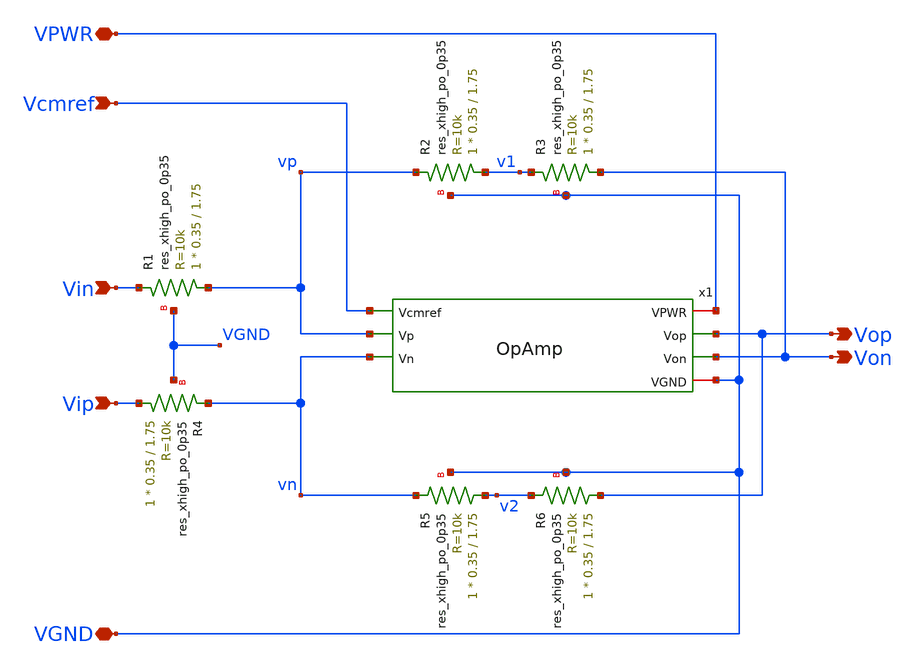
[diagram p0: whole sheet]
** sch_path: Circuits/Examples/InvAmp/InvAmp.sch
**.subckt InvAmp VPWR VGND Vcmref Vin Vip Vop Von
*.iopin VPWR
*.iopin VGND
*.ipin Vcmref
*.ipin Vin
*.ipin Vip
*.opin Vop
*.opin Von
x1 VPWR Vcmref Vop Von vp vn VGND OpAmp
XR1 vp Vin VGND sky130_fd_pr__res_xhigh_po_0p35 L=1.75 mult=1 m=1
XR2 v1 vp VGND sky130_fd_pr__res_xhigh_po_0p35 L=1.75 mult=1 m=1
XR3 Von v1 VGND sky130_fd_pr__res_xhigh_po_0p35 L=1.75 mult=1 m=1
XR4 Vip vn VGND sky130_fd_pr__res_xhigh_po_0p35 L=1.75 mult=1 m=1
XR6 Vop v2 VGND sky130_fd_pr__res_xhigh_po_0p35 L=1.75 mult=1 m=1
XR5 v2 vn VGND sky130_fd_pr__res_xhigh_po_0p35 L=1.75 mult=1 m=1
**.ends

* expanding   symbol:  /home/jakob/Documents/RALF/Circuits/Examples/OpAmp/OpAmp.sym # of pins=7
** sym_path: Circuits/Examples/OpAmp/OpAmp.sym
** sch_path: Circuits/Examples/OpAmp/OpAmp.sch
.subckt OpAmp VPWR Vcmref Vop Von Vp Vn VGND
*.opin Von
*.opin Vop
*.ipin Vcmref
*.ipin Vp
*.ipin Vn
*.iopin VPWR
*.iopin VGND
x2 VPWR Vcmref Von vcmfb Vop vbias VGND CMMFeedback
x3 VPWR vbias VGND GmBias
x1 VPWR Von vcmfb Vp Vn vbias vbias Vop VGND MillerOpAmp
.ends


* expanding   symbol:  /home/jakob/Documents/RALF/Circuits/Examples/OpAmp/CMMFeedback.sym # of
*+ pins=7
** sym_path: Circuits/Examples/OpAmp/CMMFeedback.sym
** sch_path: Circuits/Examples/OpAmp/CMMFeedback.sch
.subckt CMMFeedback Vdd Vcmref Vp Vout Vn Vbdan Vss
*.ipin Vbdan
*.opin Vout
*.ipin Vp
*.ipin Vcmref
*.ipin Vn
*.iopin Vss
*.iopin Vdd
XR1 Vp net1 Vss sky130_fd_pr__res_xhigh_po_0p35 L=3.5 mult=1 m=1
XR2 net1 net2 Vss sky130_fd_pr__res_xhigh_po_0p35 L=3.5 mult=1 m=1
XR3 net2 net3 Vss sky130_fd_pr__res_xhigh_po_0p35 L=3.5 mult=1 m=1
XR4 net3 net4 Vss sky130_fd_pr__res_xhigh_po_0p35 L=3.5 mult=1 m=1
XR5 net4 vcmi Vss sky130_fd_pr__res_xhigh_po_0p35 L=3.5 mult=1 m=1
XR6 Vn net5 Vss sky130_fd_pr__res_xhigh_po_0p35 L=3.5 mult=1 m=1
XR10 net5 net6 Vss sky130_fd_pr__res_xhigh_po_0p35 L=3.5 mult=1 m=1
XR9 net6 net7 Vss sky130_fd_pr__res_xhigh_po_0p35 L=3.5 mult=1 m=1
XR8 net7 net8 Vss sky130_fd_pr__res_xhigh_po_0p35 L=3.5 mult=1 m=1
XR7 net8 vcmi Vss sky130_fd_pr__res_xhigh_po_0p35 L=3.5 mult=1 m=1
x1 Vdd vdts Vout vdts Vcmref vcmi Vbdan Vss DiffAmp
.ends


* expanding   symbol:  /home/jakob/Documents/RALF/Circuits/Examples/OpAmp/GmBias.sym # of pins=3
** sym_path: Circuits/Examples/OpAmp/GmBias.sym
** sch_path: Circuits/Examples/OpAmp/GmBias.sch
.subckt GmBias Vdd Vbias Vss
*.opin Vbias
*.iopin Vss
*.iopin Vdd
XM6 Vbias Vbias Vss Vss sky130_fd_pr__nfet_01v8 L=2 W=1 nf=1 ad='int((nf+1)/2) * W/nf * 0.29' as='int((nf+2)/2) * W/nf * 0.29'
+ pd='2*int((nf+1)/2) * (W/nf + 0.29)' ps='2*int((nf+2)/2) * (W/nf + 0.29)' nrd='0.29 / W' nrs='0.29 / W'
+ sa=0 sb=0 sd=0 mult=1 m=1
XM2 v1 v1 Vdd Vdd sky130_fd_pr__pfet_01v8 L=1 W=4 nf=2 ad='int((nf+1)/2) * W/nf * 0.29' as='int((nf+2)/2) * W/nf * 0.29'
+ pd='2*int((nf+1)/2) * (W/nf + 0.29)' ps='2*int((nf+2)/2) * (W/nf + 0.29)' nrd='0.29 / W' nrs='0.29 / W'
+ sa=0 sb=0 sd=0 mult=1 m=1
XM1 Vbias v1 Vdd Vdd sky130_fd_pr__pfet_01v8 L=1 W=4 nf=2 ad='int((nf+1)/2) * W/nf * 0.29' as='int((nf+2)/2) * W/nf * 0.29'
+ pd='2*int((nf+1)/2) * (W/nf + 0.29)' ps='2*int((nf+2)/2) * (W/nf + 0.29)' nrd='0.29 / W' nrs='0.29 / W'
+ sa=0 sb=0 sd=0 mult=1 m=1
XM3 v1 Vbias net1 Vss sky130_fd_pr__nfet_01v8 L=2 W=1 nf=1 ad='int((nf+1)/2) * W/nf * 0.29' as='int((nf+2)/2) * W/nf * 0.29'
+ pd='2*int((nf+1)/2) * (W/nf + 0.29)' ps='2*int((nf+2)/2) * (W/nf + 0.29)' nrd='0.29 / W' nrs='0.29 / W'
+ sa=0 sb=0 sd=0 mult=1 m=1
XR6 Vss net1 Vss sky130_fd_pr__res_xhigh_po_0p35 L=1 mult=1 m=1
XM4 v1 v1 Vbias Vss sky130_fd_pr__nfet_01v8 L=2 W=1 nf=1 ad='int((nf+1)/2) * W/nf * 0.29' as='int((nf+2)/2) * W/nf * 0.29'
+ pd='2*int((nf+1)/2) * (W/nf + 0.29)' ps='2*int((nf+2)/2) * (W/nf + 0.29)' nrd='0.29 / W' nrs='0.29 / W'
+ sa=0 sb=0 sd=0 mult=1 m=1
.ends


* expanding   symbol:  /home/jakob/Documents/RALF/Circuits/Examples/OpAmp/MillerOpAmp.sym # of
*+ pins=9
** sym_path: Circuits/Examples/OpAmp/MillerOpAmp.sym
** sch_path: Circuits/Examples/OpAmp/MillerOpAmp.sch
.subckt MillerOpAmp VPWR Von Vbdap Vp Vn Vbdan Vbcsn Vop VGND
*.opin Von
*.opin Vop
*.ipin Vbcsn
*.ipin Vp
*.ipin Vn
*.ipin Vbdan
*.iopin VPWR
*.iopin VGND
*.ipin Vbdap
XC1 von1 Von sky130_fd_pr__cap_mim_m3_1 W=4 L=4 MF=1 m=1
XC2 vop1 Vop sky130_fd_pr__cap_mim_m3_1 W=4 L=4 MF=1 m=1
x1 VPWR Vbdap von1 vop1 Vp Vn Vbdan VGND DiffAmp
x2 VPWR von1 Von Vbcsn VGND CSAmp
x3 VPWR vop1 Vop Vbcsn VGND CSAmp
.ends


* expanding   symbol:  /home/jakob/Documents/RALF/Circuits/Examples/OpAmp/DiffAmp.sym # of pins=8
** sym_path: Circuits/Examples/OpAmp/DiffAmp.sym
** sch_path: Circuits/Examples/OpAmp/DiffAmp.sch
.subckt DiffAmp Vdd Vbp Von Vop Vp Vn Vbn Vss
*.iopin Vdd
*.iopin Vss
*.ipin Vp
*.ipin Vn
*.ipin Vbn
*.ipin Vbp
*.opin Vop
*.opin Von
XM1 Vop Vp vmid Vss sky130_fd_pr__nfet_01v8 L=1 W=1 nf=1 ad='int((nf+1)/2) * W/nf * 0.29' as='int((nf+2)/2) * W/nf * 0.29'
+ pd='2*int((nf+1)/2) * (W/nf + 0.29)' ps='2*int((nf+2)/2) * (W/nf + 0.29)' nrd='0.29 / W' nrs='0.29 / W'
+ sa=0 sb=0 sd=0 mult=1 m=1
XM2 Von Vn vmid Vss sky130_fd_pr__nfet_01v8 L=1 W=1 nf=1 ad='int((nf+1)/2) * W/nf * 0.29' as='int((nf+2)/2) * W/nf * 0.29'
+ pd='2*int((nf+1)/2) * (W/nf + 0.29)' ps='2*int((nf+2)/2) * (W/nf + 0.29)' nrd='0.29 / W' nrs='0.29 / W'
+ sa=0 sb=0 sd=0 mult=1 m=1
XM3 Vop Vbp Vdd Vdd sky130_fd_pr__pfet_01v8 L=1 W=2 nf=1 ad='int((nf+1)/2) * W/nf * 0.29' as='int((nf+2)/2) * W/nf * 0.29'
+ pd='2*int((nf+1)/2) * (W/nf + 0.29)' ps='2*int((nf+2)/2) * (W/nf + 0.29)' nrd='0.29 / W' nrs='0.29 / W'
+ sa=0 sb=0 sd=0 mult=1 m=1
XM4 Von Vbp Vdd Vdd sky130_fd_pr__pfet_01v8 L=1 W=2 nf=1 ad='int((nf+1)/2) * W/nf * 0.29' as='int((nf+2)/2) * W/nf * 0.29'
+ pd='2*int((nf+1)/2) * (W/nf + 0.29)' ps='2*int((nf+2)/2) * (W/nf + 0.29)' nrd='0.29 / W' nrs='0.29 / W'
+ sa=0 sb=0 sd=0 mult=1 m=1
XM5 vmid Vbn Vss Vss sky130_fd_pr__nfet_01v8 L=2 W=1 nf=1 ad='int((nf+1)/2) * W/nf * 0.29' as='int((nf+2)/2) * W/nf * 0.29'
+ pd='2*int((nf+1)/2) * (W/nf + 0.29)' ps='2*int((nf+2)/2) * (W/nf + 0.29)' nrd='0.29 / W' nrs='0.29 / W'
+ sa=0 sb=0 sd=0 mult=1 m=1
.ends


* expanding   symbol:  /home/jakob/Documents/RALF/Circuits/Examples/OpAmp/CSAmp.sym # of pins=5
** sym_path: Circuits/Examples/OpAmp/CSAmp.sym
** sch_path: Circuits/Examples/OpAmp/CSAmp.sch
.subckt CSAmp Vdd Vi Vo Vbn Vss
*.ipin Vbn
*.ipin Vi
*.iopin Vdd
*.iopin Vss
*.opin Vo
XM1 Vo Vi Vdd Vdd sky130_fd_pr__pfet_01v8 L=1 W=8 nf=1 ad='int((nf+1)/2) * W/nf * 0.29' as='int((nf+2)/2) * W/nf * 0.29'
+ pd='2*int((nf+1)/2) * (W/nf + 0.29)' ps='2*int((nf+2)/2) * (W/nf + 0.29)' nrd='0.29 / W' nrs='0.29 / W'
+ sa=0 sb=0 sd=0 mult=1 m=1
XM2 Vo Vbn Vss Vss sky130_fd_pr__nfet_01v8 L=2 W=10 nf=1 ad='int((nf+1)/2) * W/nf * 0.29' as='int((nf+2)/2) * W/nf * 0.29'
+ pd='2*int((nf+1)/2) * (W/nf + 0.29)' ps='2*int((nf+2)/2) * (W/nf + 0.29)' nrd='0.29 / W' nrs='0.29 / W'
+ sa=0 sb=0 sd=0 mult=1 m=1
XM3 Vo Vi Vdd Vdd sky130_fd_pr__pfet_01v8 L=1 W=8 nf=1 ad='int((nf+1)/2) * W/nf * 0.29' as='int((nf+2)/2) * W/nf * 0.29'
+ pd='2*int((nf+1)/2) * (W/nf + 0.29)' ps='2*int((nf+2)/2) * (W/nf + 0.29)' nrd='0.29 / W' nrs='0.29 / W'
+ sa=0 sb=0 sd=0 mult=1 m=1
XM4 Vo Vbn Vss Vss sky130_fd_pr__nfet_01v8 L=2 W=10 nf=1 ad='int((nf+1)/2) * W/nf * 0.29' as='int((nf+2)/2) * W/nf * 0.29'
+ pd='2*int((nf+1)/2) * (W/nf + 0.29)' ps='2*int((nf+2)/2) * (W/nf + 0.29)' nrd='0.29 / W' nrs='0.29 / W'
+ sa=0 sb=0 sd=0 mult=1 m=1
.ends

.end
